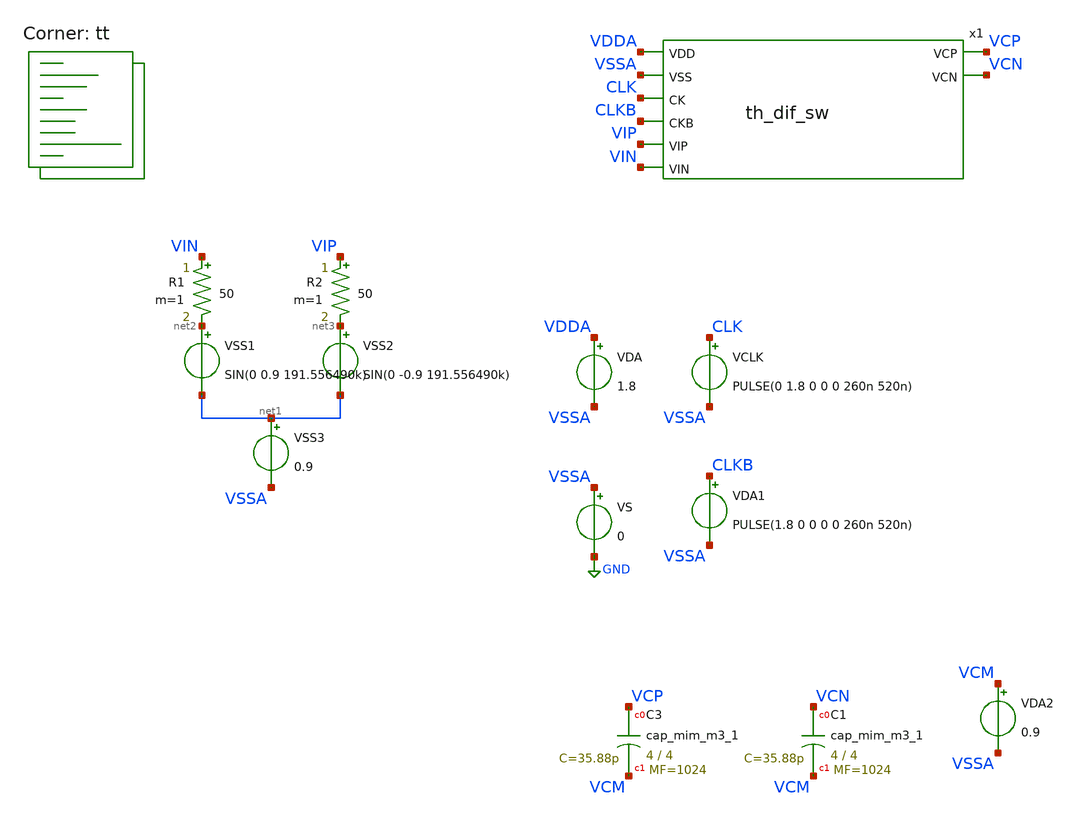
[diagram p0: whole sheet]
** sch_path: xschem/th_tb.sch
**.subckt th_tb
VS VSSA GND 0
VDA VDDA VSSA 1.8
VSS1 net2 net1 SIN(0 0.9 191.556490k)
VSS2 net3 net1 SIN(0 -0.9 191.556490k)
VSS3 net1 VSSA 0.9
VCLK CLK VSSA PULSE(0 1.8 0 0 0 260n 520n)
R1 VIN net2 50 m=1
R2 VIP net3 50 m=1
VDA1 CLKB VSSA PULSE(1.8 0 0 0 0 260n 520n)
x1 VDDA VSSA CLK CLKB VIP VIN VCP VCN th_dif_sw
VDA2 VCM VSSA 0.9
XC3 VCP VCM sky130_fd_pr__cap_mim_m3_1 W=4 L=4 MF=1024 m=1024
XC1 VCN VCM sky130_fd_pr__cap_mim_m3_1 W=4 L=4 MF=1024 m=1024
**** begin user architecture code

** opencircuitdesign pdks install
* .lib $::SKYWATER_MODELS/sky130.lib.spice tt
.include $PDK_ROOT/$PDK/libs.ref/sky130_fd_sc_hd/spice/sky130_fd_sc_hd.spice



.option wnflag=0 bypass=1
.options method=gear rawfile=binary
.options solver=klu nomod
.control
set num_threads=6
save CLK CLKB VIP VIN VCP VCN
global netlist_dir .
set wr_singlescale
tran 100p 535u  ; Mengubah start time menjadi 1n
remzerovec
write th_tb.raw
wrdata th_tb.txt CLK CLKB VIP VIN VCP VCN
quit 0
.endc

.lib $::SKYWATER_MODELS/sky130.lib.spice tt
**** end user architecture code
**.ends

* expanding   symbol:  th_dif_sw.sym # of pins=8
** sym_path: xschem/th_dif_sw.sym
** sch_path: xschem/th_dif_sw.sch
.subckt th_dif_sw VDD VSS CK CKB VIP VIN VCP VCN
*.ipin VDD
*.ipin VSS
*.ipin CK
*.ipin CKB
*.ipin VIP
*.ipin VIN
*.opin VCP
*.opin VCN
x1 VDD VSS CK_BUFF CKB_BUFF VIP VCP th_sw
x2 VDD VSS CK_BUFF CKB_BUFF VIN VCN th_sw
x3 CK VSS VSS VDD VDD CK_BUFF sky130_fd_sc_hs__buf_16
x4 CKB VSS VSS VDD VDD CKB_BUFF sky130_fd_sc_hs__buf_16
**** begin user architecture code

.include /usr/local/share/pdk/sky130A/libs.ref/sky130_fd_sc_hs/spice/sky130_fd_sc_hs.spice

**** end user architecture code
.ends


* expanding   symbol:  th_sw.sym # of pins=6
** sym_path: xschem/th_sw.sym
** sch_path: xschem/th_sw.sch
.subckt th_sw VDD VSS CK CKB IN OUT
*.ipin VDD
*.ipin VSS
*.ipin CK
*.ipin CKB
*.ipin IN
*.opin OUT
XM1 net1 CKB VDD VDD sky130_fd_pr__pfet_01v8 L=0.15 W=3 nf=1 ad='int((nf+1)/2) * W/nf * 0.29' as='int((nf+2)/2) * W/nf * 0.29'
+ pd='2*int((nf+1)/2) * (W/nf + 0.29)' ps='2*int((nf+2)/2) * (W/nf + 0.29)' nrd='0.29 / W' nrs='0.29 / W'
+ sa=0 sb=0 sd=0 mult=1 m=1
XM2 net2 VGS VDD net2 sky130_fd_pr__pfet_01v8 L=0.15 W=1 nf=1 ad='int((nf+1)/2) * W/nf * 0.29' as='int((nf+2)/2) * W/nf * 0.29'
+ pd='2*int((nf+1)/2) * (W/nf + 0.29)' ps='2*int((nf+2)/2) * (W/nf + 0.29)' nrd='0.29 / W' nrs='0.29 / W'
+ sa=0 sb=0 sd=0 mult=1 m=1
XM3 VGS net1 net2 net2 sky130_fd_pr__pfet_01v8 L=0.15 W=1 nf=1 ad='int((nf+1)/2) * W/nf * 0.29' as='int((nf+2)/2) * W/nf * 0.29'
+ pd='2*int((nf+1)/2) * (W/nf + 0.29)' ps='2*int((nf+2)/2) * (W/nf + 0.29)' nrd='0.29 / W' nrs='0.29 / W'
+ sa=0 sb=0 sd=0 mult=1 m=1
XM4 net1 CKB net4 VSS sky130_fd_pr__nfet_01v8 L=0.15 W=1 nf=1 ad='int((nf+1)/2) * W/nf * 0.29' as='int((nf+2)/2) * W/nf * 0.29'
+ pd='2*int((nf+1)/2) * (W/nf + 0.29)' ps='2*int((nf+2)/2) * (W/nf + 0.29)' nrd='0.29 / W' nrs='0.29 / W'
+ sa=0 sb=0 sd=0 mult=1 m=1
XM5 net4 CK VSS VSS sky130_fd_pr__nfet_01v8 L=0.15 W=1 nf=1 ad='int((nf+1)/2) * W/nf * 0.29' as='int((nf+2)/2) * W/nf * 0.29'
+ pd='2*int((nf+1)/2) * (W/nf + 0.29)' ps='2*int((nf+2)/2) * (W/nf + 0.29)' nrd='0.29 / W' nrs='0.29 / W'
+ sa=0 sb=0 sd=0 mult=1 m=1
XM6 net1 VGS net4 VSS sky130_fd_pr__nfet_01v8 L=0.15 W=1 nf=1 ad='int((nf+1)/2) * W/nf * 0.29' as='int((nf+2)/2) * W/nf * 0.29'
+ pd='2*int((nf+1)/2) * (W/nf + 0.29)' ps='2*int((nf+2)/2) * (W/nf + 0.29)' nrd='0.29 / W' nrs='0.29 / W'
+ sa=0 sb=0 sd=0 mult=1 m=1
XM7 IN VGS net4 VSS sky130_fd_pr__nfet_01v8 L=0.15 W=1 nf=1 ad='int((nf+1)/2) * W/nf * 0.29' as='int((nf+2)/2) * W/nf * 0.29'
+ pd='2*int((nf+1)/2) * (W/nf + 0.29)' ps='2*int((nf+2)/2) * (W/nf + 0.29)' nrd='0.29 / W' nrs='0.29 / W'
+ sa=0 sb=0 sd=0 mult=1 m=1
XM8 VGS VDD net3 VSS sky130_fd_pr__nfet_01v8 L=0.15 W=1 nf=1 ad='int((nf+1)/2) * W/nf * 0.29' as='int((nf+2)/2) * W/nf * 0.29'
+ pd='2*int((nf+1)/2) * (W/nf + 0.29)' ps='2*int((nf+2)/2) * (W/nf + 0.29)' nrd='0.29 / W' nrs='0.29 / W'
+ sa=0 sb=0 sd=0 mult=1 m=1
XM9 net3 CK VSS VSS sky130_fd_pr__nfet_01v8 L=0.15 W=1 nf=1 ad='int((nf+1)/2) * W/nf * 0.29' as='int((nf+2)/2) * W/nf * 0.29'
+ pd='2*int((nf+1)/2) * (W/nf + 0.29)' ps='2*int((nf+2)/2) * (W/nf + 0.29)' nrd='0.29 / W' nrs='0.29 / W'
+ sa=0 sb=0 sd=0 mult=1 m=1
XC1 net2 net4 sky130_fd_pr__cap_mim_m3_1 W=4 L=4 MF=8 m=8
XM10 OUT VGS IN VSS sky130_fd_pr__nfet_01v8 L=0.15 W=8 nf=1 ad='int((nf+1)/2) * W/nf * 0.29' as='int((nf+2)/2) * W/nf * 0.29'
+ pd='2*int((nf+1)/2) * (W/nf + 0.29)' ps='2*int((nf+2)/2) * (W/nf + 0.29)' nrd='0.29 / W' nrs='0.29 / W'
+ sa=0 sb=0 sd=0 mult=1 m=1
XM11 IN CK IN VSS sky130_fd_pr__nfet_01v8 L=0.15 W=8 nf=1 ad='int((nf+1)/2) * W/nf * 0.29' as='int((nf+2)/2) * W/nf * 0.29'
+ pd='2*int((nf+1)/2) * (W/nf + 0.29)' ps='2*int((nf+2)/2) * (W/nf + 0.29)' nrd='0.29 / W' nrs='0.29 / W'
+ sa=0 sb=0 sd=0 mult=1 m=1
XM12 OUT CK OUT VSS sky130_fd_pr__nfet_01v8 L=0.15 W=8 nf=1 ad='int((nf+1)/2) * W/nf * 0.29' as='int((nf+2)/2) * W/nf * 0.29'
+ pd='2*int((nf+1)/2) * (W/nf + 0.29)' ps='2*int((nf+2)/2) * (W/nf + 0.29)' nrd='0.29 / W' nrs='0.29 / W'
+ sa=0 sb=0 sd=0 mult=1 m=1
.ends

.GLOBAL GND
.end
